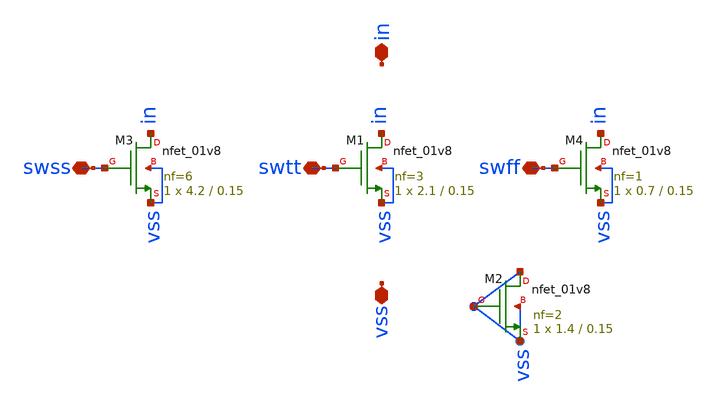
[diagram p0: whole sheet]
** sch_path: xschem/current_tails_1.sch
**.subckt current_tails_1 in vss swtt swff swss
*.iopin in
*.iopin vss
*.iopin swtt
*.iopin swff
*.iopin swss
XM4 in swff vss vss sky130_fd_pr__nfet_01v8 L=0.15 W=0.7 nf=1 ad='int((nf+1)/2) * W/nf * 0.29' as='int((nf+2)/2) * W/nf * 0.29'
+ pd='2*int((nf+1)/2) * (W/nf + 0.29)' ps='2*int((nf+2)/2) * (W/nf + 0.29)' nrd='0.29 / W' nrs='0.29 / W'
+ sa=0 sb=0 sd=0 mult=1 m=1
XM1 in swtt vss vss sky130_fd_pr__nfet_01v8 L=0.15 W=2.1 nf=3 ad='int((nf+1)/2) * W/nf * 0.29' as='int((nf+2)/2) * W/nf * 0.29'
+ pd='2*int((nf+1)/2) * (W/nf + 0.29)' ps='2*int((nf+2)/2) * (W/nf + 0.29)' nrd='0.29 / W' nrs='0.29 / W'
+ sa=0 sb=0 sd=0 mult=1 m=1
XM3 in swss vss vss sky130_fd_pr__nfet_01v8 L=0.15 W=4.2 nf=6 ad='int((nf+1)/2) * W/nf * 0.29' as='int((nf+2)/2) * W/nf * 0.29'
+ pd='2*int((nf+1)/2) * (W/nf + 0.29)' ps='2*int((nf+2)/2) * (W/nf + 0.29)' nrd='0.29 / W' nrs='0.29 / W'
+ sa=0 sb=0 sd=0 mult=1 m=1
XM2 vss vss vss vss sky130_fd_pr__nfet_01v8 L=0.15 W=1.4 nf=2 ad='int((nf+1)/2) * W/nf * 0.29' as='int((nf+2)/2) * W/nf * 0.29'
+ pd='2*int((nf+1)/2) * (W/nf + 0.29)' ps='2*int((nf+2)/2) * (W/nf + 0.29)' nrd='0.29 / W' nrs='0.29 / W'
+ sa=0 sb=0 sd=0 mult=1 m=1
**.ends
.end
